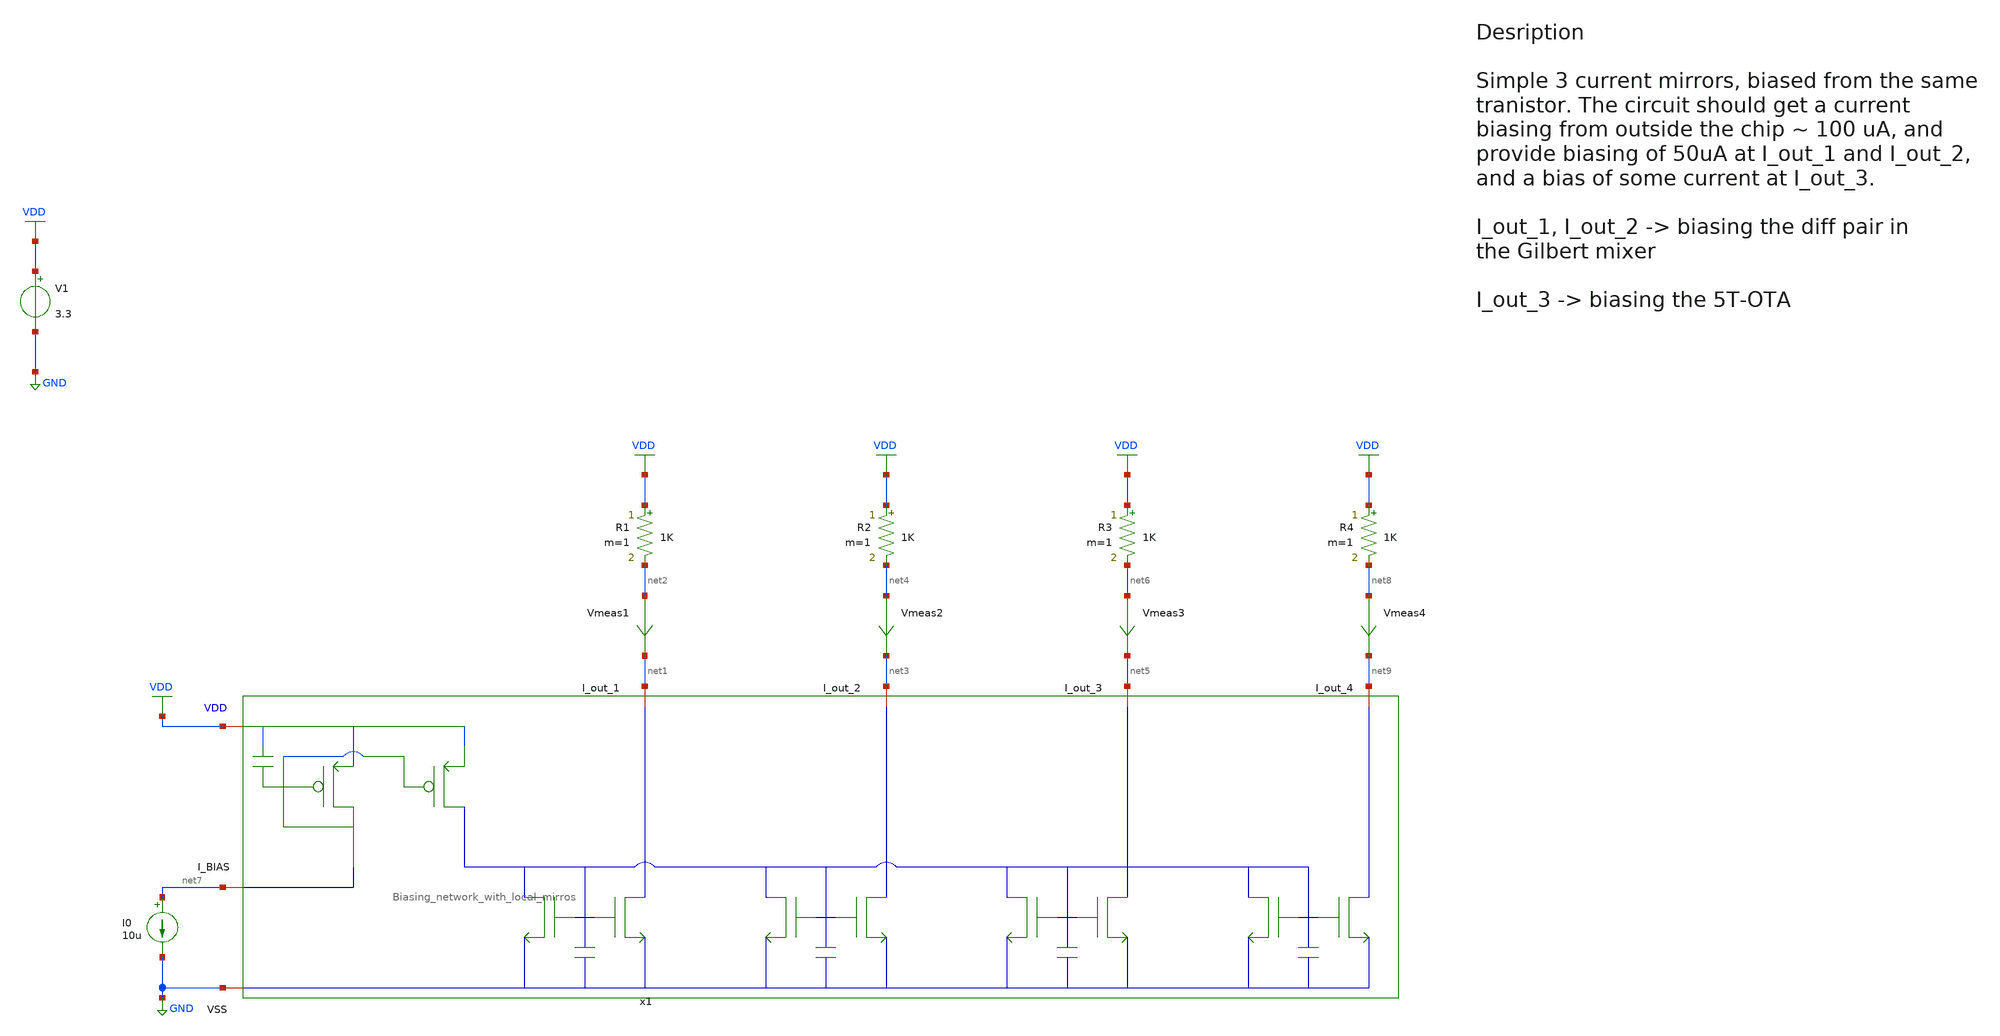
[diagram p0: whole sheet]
** sch_path: src/design_tb/Local_mirror_biasing_tb.sch
**.subckt Local_mirror_biasing_tb
I0 net7 GND 10u
V1 VDD GND 3.3
Vmeas1 net2 net1 0
.save i(vmeas1)
Vmeas2 net4 net3 0
.save i(vmeas2)
Vmeas3 net6 net5 0
.save i(vmeas3)
R1 VDD net2 1K m=1
R2 VDD net4 1K m=1
R3 VDD net6 1K m=1
x1 VDD net1 net3 net5 net7 GND net9 Biasing_network_with_local_mirros pmos_l_ref=0.4u pmos_w_ref=2u
+ pmos_l_mir=0.4u pmos_w_mir=8u nmos_l_ref_1=1u nmos_w_ref_1=1.5u nmos_nf_ref_1=1 nmos_l_mir_1=1u nmos_w_mir_1=7.5u
+ nmos_nf_mir_1=5 nmos_l_ref_2=1u nmos_w_ref_2=1.5u nmos_nf_ref_2=1 nmos_l_mir_2=1u nmos_w_mir_2=7.5u nmos_nf_mir_2=5
+ nmos_l_ref_3=1u nmos_w_ref_3=1.5u nmos_nf_ref_3=2 nmos_l_mir_3=1u nmos_w_mir_3=1.5u nmos_nf_mir_3=2 nmos_l_ref_4=1u
+ nmos_w_ref_4=1.5u nmos_nf_ref_4=1 nmos_l_mir_4=1u nmos_w_mir_4=15u nmos_nf_mir_4=10
Vmeas4 net8 net9 0
.save i(vmeas4)
R4 VDD net8 1K m=1
**** begin user architecture code

.include $::180MCU_MODELS/design.ngspice
.lib $::180MCU_MODELS/sm141064.ngspice typical
.lib $::180MCU_MODELS/sm141064.ngspice mimcap_typical
.lib $::180MCU_MODELS/sm141064.ngspice cap_mim
.lib $::180MCU_MODELS/sm141064.ngspice res_typical
.lib $::180MCU_MODELS/sm141064.ngspice diode_typical
.lib $::180MCU_MODELS/sm141064.ngspice bjt_typical
.lib $::180MCU_MODELS/sm141064.ngspice moscap_typical
.lib $::180MCU_MODELS/sm141064.ngspice mimcap_typical



* Add convergence aids
.option method=gear

.control

    * operating point
    op
    show

    write Local_mirror_biasing_tb.raw

    set appendwrite

    * Transient analysis to observe mixing operation
    tran 1n 0.01u
    write Local_mirror_biasing_tb.raw

.endc


**** end user architecture code
**.ends
.GLOBAL GND
.GLOBAL VDD
.end
